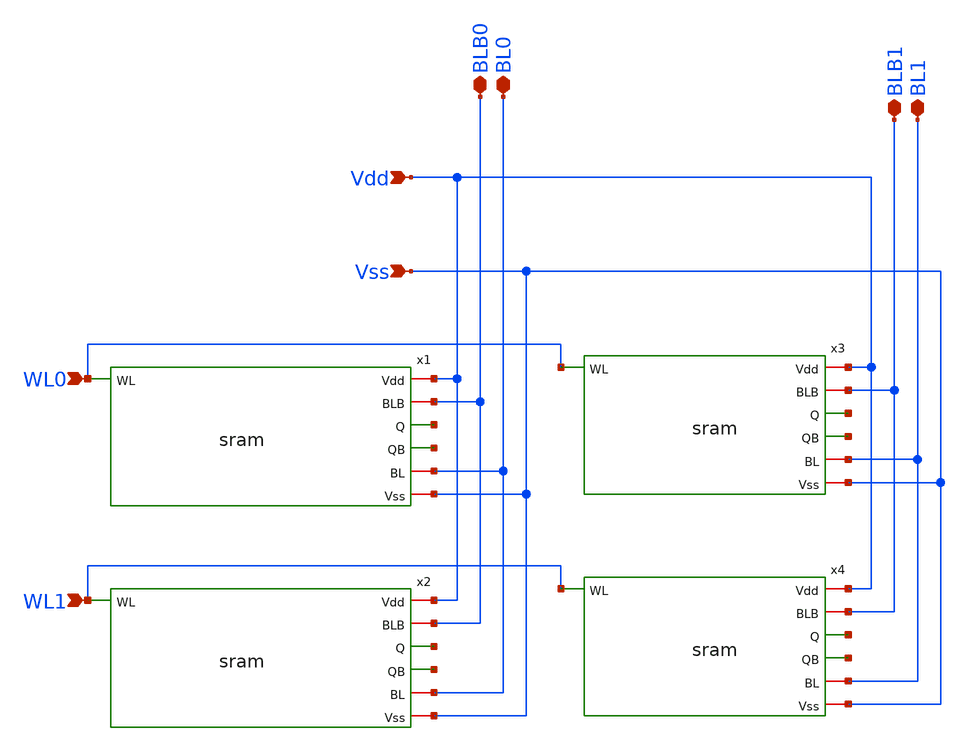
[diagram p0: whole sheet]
** sch_path: sram_array.sch
**.subckt sram_array WL1 Vdd Vss BL0 BLB0 BL1 BLB1 WL0
*.ipin WL1
*.ipin Vdd
*.ipin Vss
*.iopin BL0
*.iopin BLB0
*.iopin BL1
*.iopin BLB1
*.ipin WL0
x1 WL0 Vdd BLB0 net1 net2 BL0 Vss sram
x2 WL1 Vdd BLB0 net3 net4 BL0 Vss sram
x3 WL0 Vdd BLB1 net5 net6 BL1 Vss sram
x4 WL1 Vdd BLB1 net7 net8 BL1 Vss sram
**.ends

* expanding   symbol:  sram.sym # of pins=7
** sym_path: sram.sym
** sch_path: sram.sch
.subckt sram WL Vdd BLB Q QB BL Vss
*.iopin Vdd
*.iopin Vss
*.iopin BLB
*.iopin BL
*.ipin WL
*.opin Q
*.opin QB
XXM1 Q QB Vss Vss NMOS w=3.4u l=1u nrd=0 nrs=0 m=1
XXM2 Q QB Vdd Vdd PMOS w=3.4u l=1u nrd=0 nrs=0 m=1
XXM3 QB Q Vss Vss NMOS w=3.4u l=1u nrd=0 nrs=0 m=1
XXM4 QB Q Vdd Vdd PMOS w=3.4u l=1u nrd=0 nrs=0 m=1
XXM7 Q WL BL Vss NMOS w=3.4u l=1u nrd=0 nrs=0 m=1
XXM6 QB WL BLB Vss NMOS w=3.4u l=1u nrd=0 nrs=0 m=1
.ends

.end
